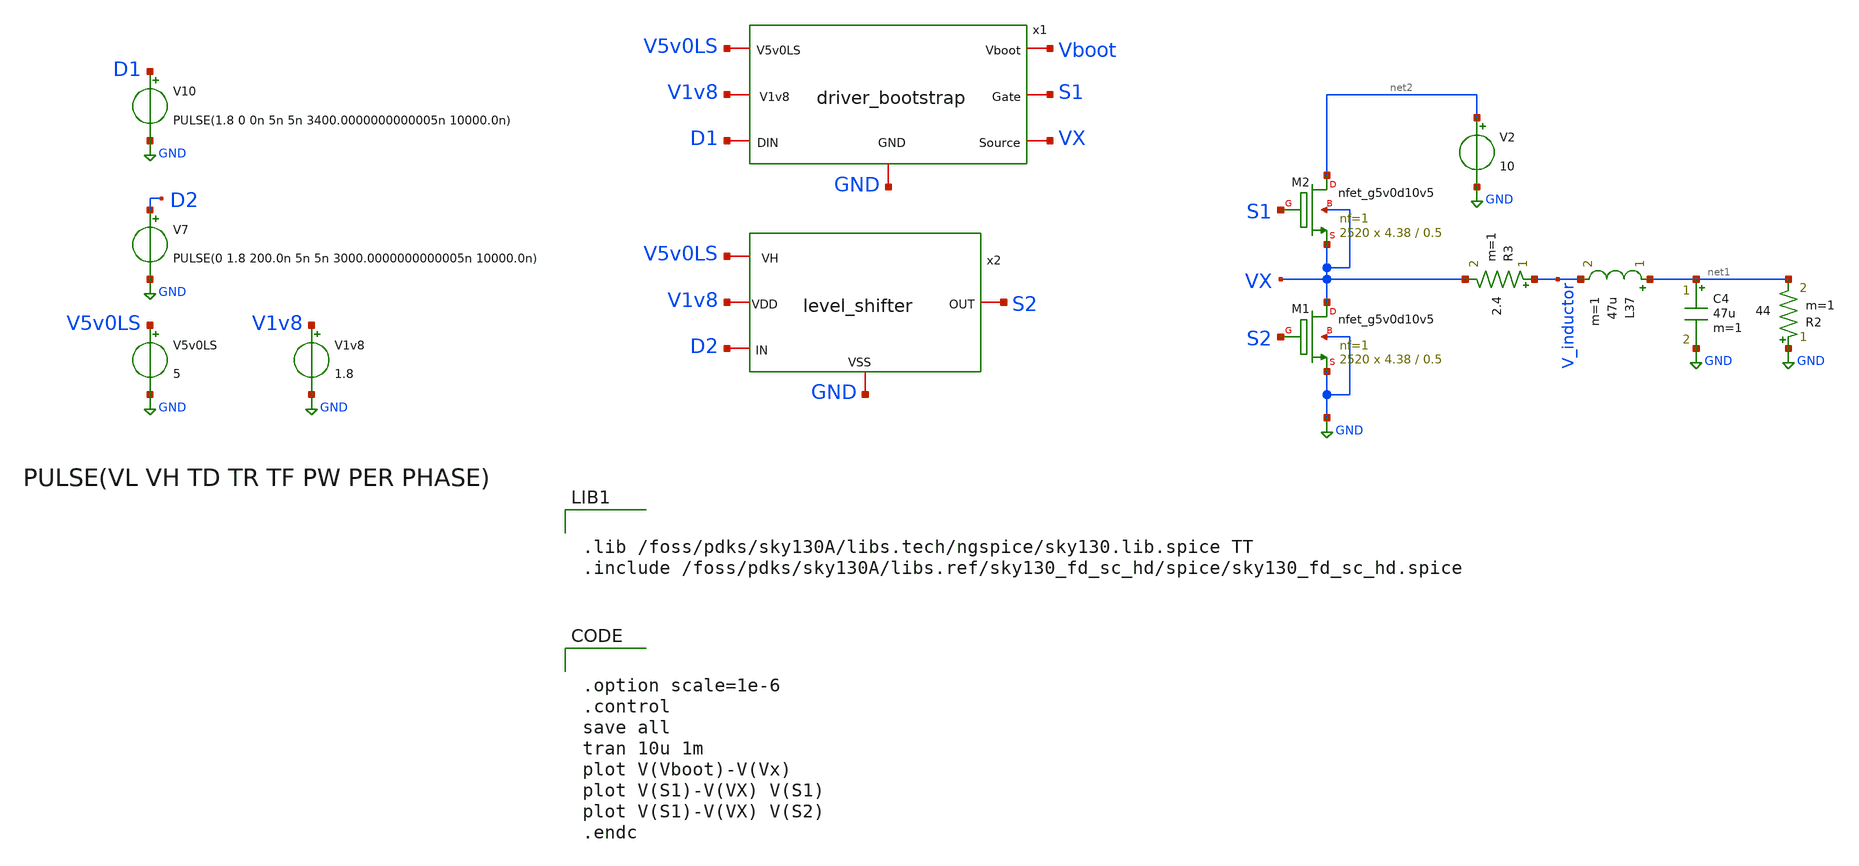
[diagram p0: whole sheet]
** sch_path: xschem/test/tb_buck_bootstrap.sch
**.subckt tb_buck_bootstrap
V5v0LS V5v0LS GND 5
V2 net2 GND 10
V1v8 V1v8 GND 1.8
V10 D1 GND PULSE(1.8 0 0n 5n 5n 3400.0000000000005n 10000.0n)
x1 Vboot S1 VX V5v0LS V1v8 GND D1 driver_bootstrap
L37 net1 V_inductor 47u m=1
R3 V_inductor VX 2.4 m=1
XM1 VX S2 GND GND sky130_fd_pr__nfet_g5v0d10v5 L=0.5 W=4.38 nf=1 ad='int((nf+1)/2) * W/nf * 0.29' as='int((nf+2)/2) * W/nf * 0.29'
+ pd='2*int((nf+1)/2) * (W/nf + 0.29)' ps='2*int((nf+2)/2) * (W/nf + 0.29)' nrd='0.29 / W' nrs='0.29 / W'
+ sa=0 sb=0 sd=0 mult=2520 m=2520
XM2 net2 S1 VX VX sky130_fd_pr__nfet_g5v0d10v5 L=0.5 W=4.38 nf=1 ad='int((nf+1)/2) * W/nf * 0.29' as='int((nf+2)/2) * W/nf * 0.29'
+ pd='2*int((nf+1)/2) * (W/nf + 0.29)' ps='2*int((nf+2)/2) * (W/nf + 0.29)' nrd='0.29 / W' nrs='0.29 / W'
+ sa=0 sb=0 sd=0 mult=2520 m=2520
C4 net1 GND 47u m=1
R2 GND net1 44 m=1
V7 D2 GND PULSE(0 1.8 200.0n 5n 5n 3000.0000000000005n 10000.0n)
x2 V5v0LS V1v8 S2 D2 GND level_shifter
**** begin user architecture code


.lib /foss/pdks/sky130A/libs.tech/ngspice/sky130.lib.spice TT
.include /foss/pdks/sky130A/libs.ref/sky130_fd_sc_hd/spice/sky130_fd_sc_hd.spice




.option scale=1e-6
.control
save all
tran 10u 1m
plot V(Vboot)-V(Vx)
plot V(S1)-V(VX) V(S1)
plot V(S1)-V(VX) V(S2)
.endc


**** end user architecture code
**.ends
.GLOBAL GND
.end
